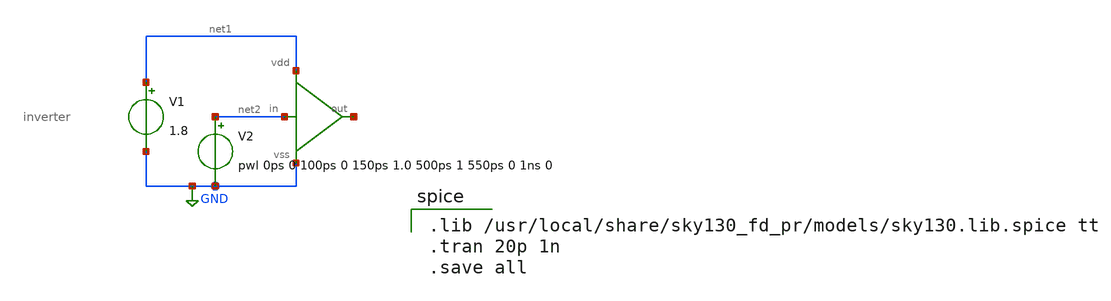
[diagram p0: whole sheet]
** sch_path: projects/and_with_inv_1/and_with_inv.sch
**.subckt and_with_inv
V1 net1 GND 1.8
x1 net3 GND net1 net2 inverter
V2 net2 GND pwl 0ps 0 100ps 0 150ps 1.0 500ps 1 550ps 0 1ns 0
**** begin user architecture code

.lib /usr/local/share/sky130_fd_pr/models/sky130.lib.spice tt
.tran 20p 1n
.save all

**** end user architecture code
**.ends

* expanding   symbol:  inverter.sym # of pins=4
** sym_path: projects/custom_lib/inverter.sym
** sch_path: projects/custom_lib/inverter.sch
.subckt inverter out vss vdd in
*.ipin in
*.ipin vdd
*.ipin vss
*.opin out
XM2 out in vss vss sky130_fd_pr__nfet_01v8 L=0.15 W=1 nf=1 ad='W * 0.29' as='W * 0.29' pd='W + 2 * 0.29'
+ ps='W + 2 * 0.29' nrd=0 nrs=0 sa=0 sb=0 sd=0 mult=1 m=1
XM1 out in vdd vdd sky130_fd_pr__pfet_01v8 L=0.15 W=1 nf=1 ad='W * 0.29' as='W * 0.29' pd='W + 2 * 0.29'
+ ps='W + 2 * 0.29' nrd=0 nrs=0 sa=0 sb=0 sd=0 mult=1 m=1
.ends

.GLOBAL GND
.end
